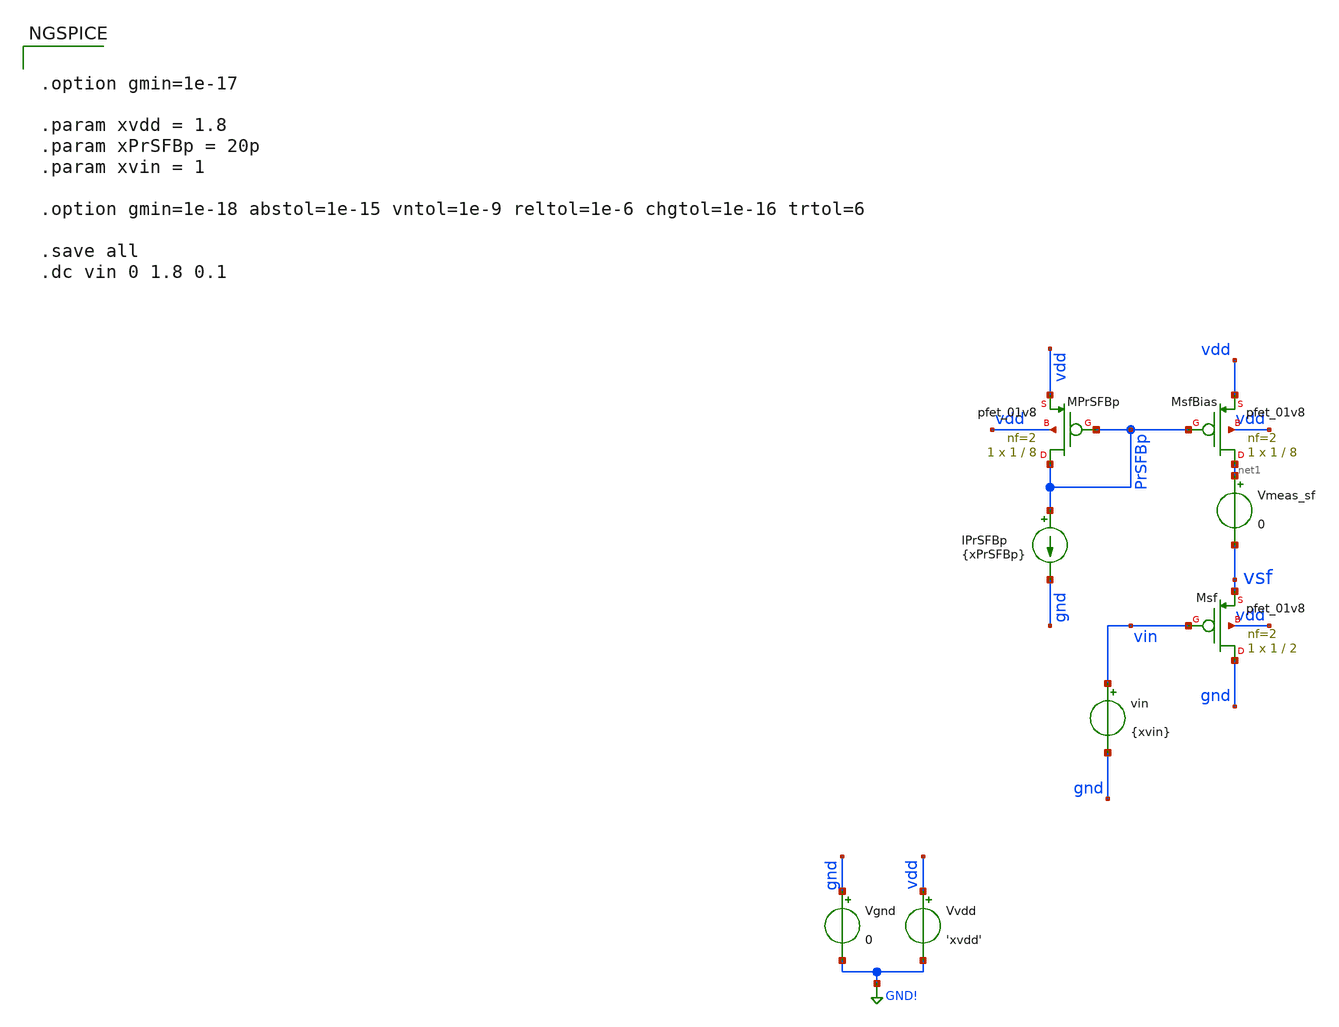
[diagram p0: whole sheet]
** sch_path: analog/klayout/production/final_merge_20260923/testbenches/cace/analog/xschem/debug_sf.sch
**.subckt debug_sf
XMsfBias net1 PrSFBp vdd vdd sky130_fd_pr__pfet_01v8 L=8 W=1 nf=2 ad='int((2 + 1)/2) * 1 / 2 * 0.29'
+ as='int((2 + 2)/2) * 1 / 2 * 0.29' pd='2*int((2 + 1)/2) * (1 / 2 + 0.29)' ps='2*int((2 + 2)/2) * (1 / 2 + 0.29)'
+ nrd='0.29 / 1 ' nrs='0.29 / 1 ' sa=0 sb=0 sd=0 mult=1 m=1
XMsf gnd vin vsf vdd sky130_fd_pr__pfet_01v8 L=2 W=1 nf=2 ad='int((2 + 1)/2) * 1 / 2 * 0.29' as='int((2 + 2)/2) * 1 / 2 * 0.29'
+ pd='2*int((2 + 1)/2) * (1 / 2 + 0.29)' ps='2*int((2 + 2)/2) * (1 / 2 + 0.29)' nrd='0.29 / 1 ' nrs='0.29 / 1 '
+ sa=0 sb=0 sd=0 mult=1 m=1
Vmeas_sf net1 vsf 0
IPrSFBp PrSFBp gnd {xPrSFBp}
XMPrSFBp PrSFBp PrSFBp vdd vdd sky130_fd_pr__pfet_01v8 L=8 W=1 nf=2 ad='int((2 + 1)/2) * 1 / 2 * 0.29'
+ as='int((2 + 2)/2) * 1 / 2 * 0.29' pd='2*int((2 + 1)/2) * (1 / 2 + 0.29)' ps='2*int((2 + 2)/2) * (1 / 2 + 0.29)'
+ nrd='0.29 / 1 ' nrs='0.29 / 1 ' sa=0 sb=0 sd=0 mult=1 m=1
vin vin gnd {xvin}
.save i(vin)
Vgnd gnd GND! 0
.save i(vgnd)
Vvdd vdd GND! 'xvdd'
.save i(vvdd)
**** begin user architecture code


.option gmin=1e-17

.param xvdd = 1.8
.param xPrSFBp = 20p
.param xvin = 1

.option gmin=1e-18 abstol=1e-15 vntol=1e-9 reltol=1e-6 chgtol=1e-16 trtol=6

.save all
.dc vin 0 1.8 0.1



** opencircuitdesign pdks install
.lib $::SKYWATER_MODELS/sky130.lib.spice tt

**** end user architecture code
**.ends
.GLOBAL GND!
.end
